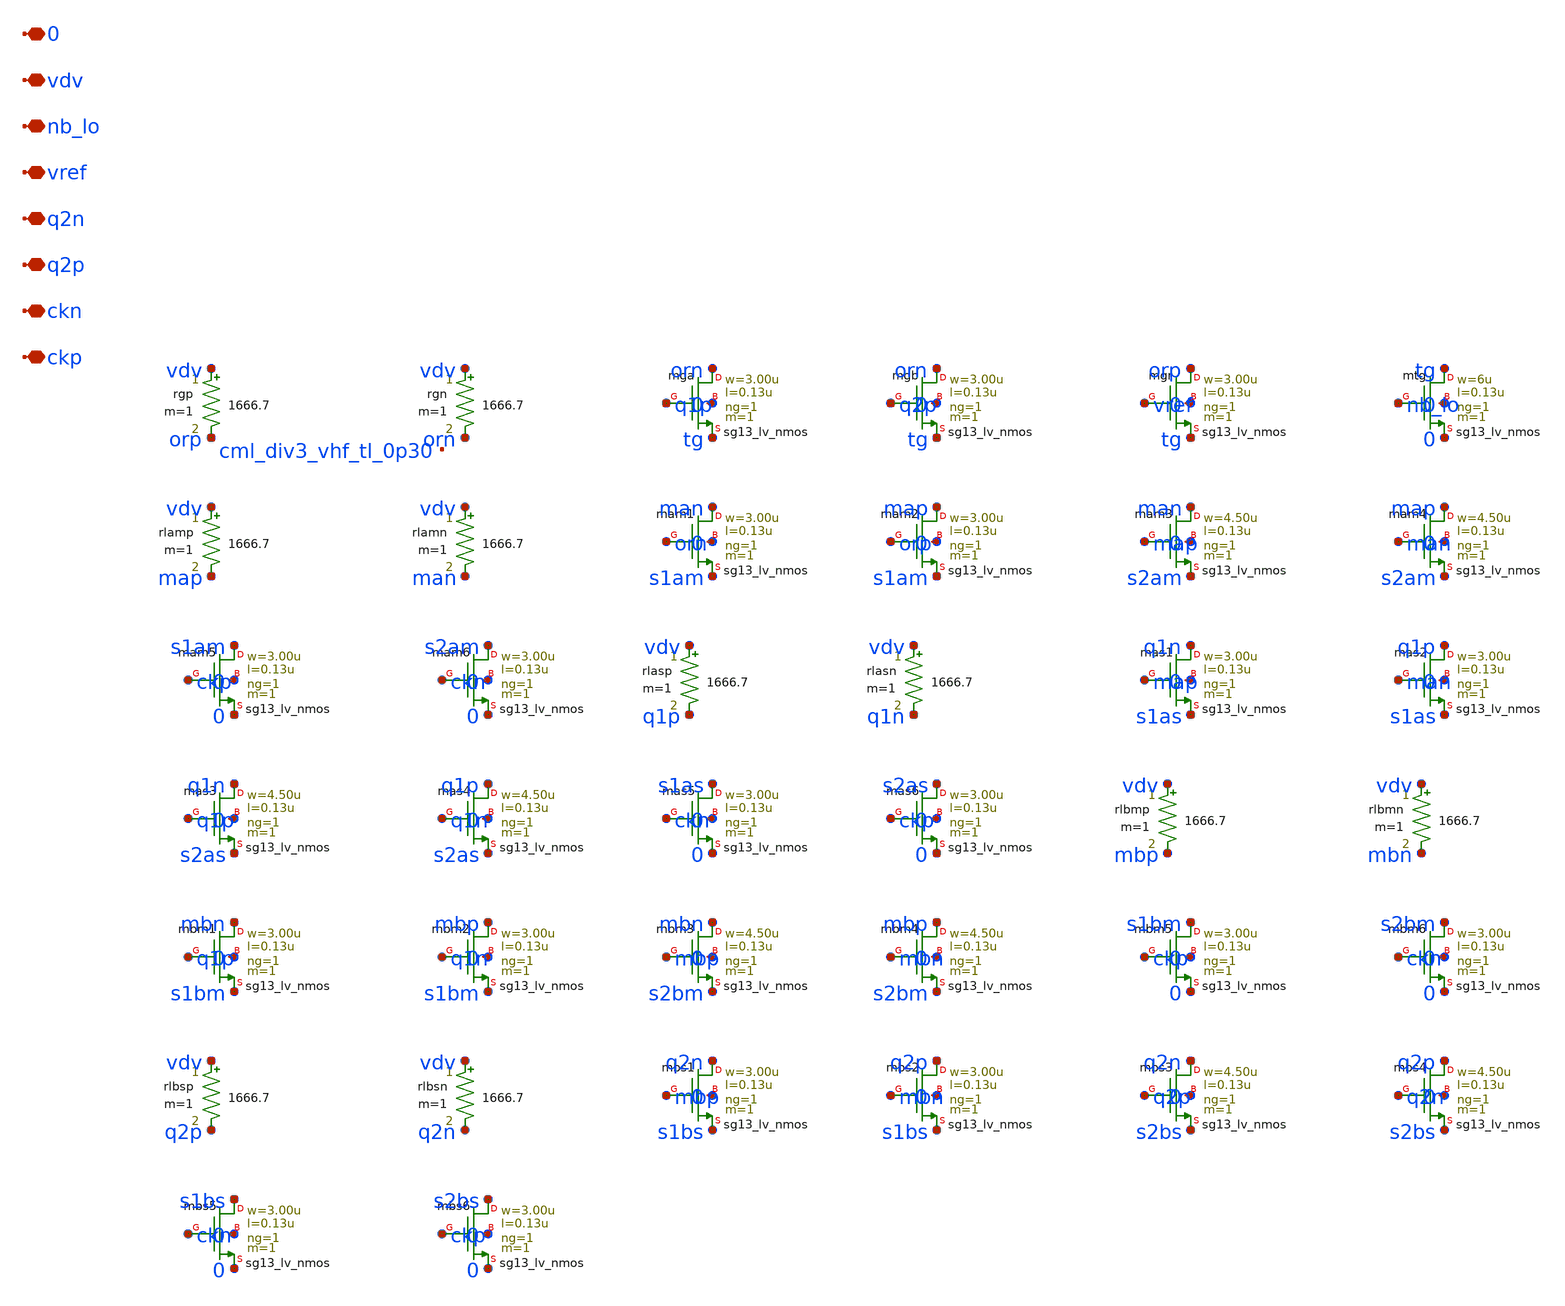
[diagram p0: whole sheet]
** sch_path: analog/lo/sch/cml_div3_vhf.sch
**.subckt cml_div3_vhf ckp ckn q2p q2n vref nb_lo vdv 0
*.iopin ckp
*.iopin ckn
*.iopin q2p
*.iopin q2n
*.iopin vref
*.iopin nb_lo
*.iopin vdv
*.iopin 0
rgp vdv orp 1666.7 m=1
rgn vdv orn 1666.7 m=1
Xmga orn q1p tg 0 sg13_lv_nmos w=3.00u l=0.13u ng=1 m=1 mm_ok=1
Xmgb orn q2p tg 0 sg13_lv_nmos w=3.00u l=0.13u ng=1 m=1 mm_ok=1
Xmgr orp vref tg 0 sg13_lv_nmos w=3.00u l=0.13u ng=1 m=1 mm_ok=1
Xmtg tg nb_lo 0 0 sg13_lv_nmos w=6u l=0.13u ng=1 m=1 mm_ok=1
rlamp vdv map 1666.7 m=1
rlamn vdv man 1666.7 m=1
Xmam1 man orn s1am 0 sg13_lv_nmos w=3.00u l=0.13u ng=1 m=1 mm_ok=1
Xmam2 map orp s1am 0 sg13_lv_nmos w=3.00u l=0.13u ng=1 m=1 mm_ok=1
Xmam3 man map s2am 0 sg13_lv_nmos w=4.50u l=0.13u ng=1 m=1 mm_ok=1
Xmam4 map man s2am 0 sg13_lv_nmos w=4.50u l=0.13u ng=1 m=1 mm_ok=1
Xmam5 s1am ckp 0 0 sg13_lv_nmos w=3.00u l=0.13u ng=1 m=1 mm_ok=1
Xmam6 s2am ckn 0 0 sg13_lv_nmos w=3.00u l=0.13u ng=1 m=1 mm_ok=1
rlasp vdv q1p 1666.7 m=1
rlasn vdv q1n 1666.7 m=1
Xmas1 q1n map s1as 0 sg13_lv_nmos w=3.00u l=0.13u ng=1 m=1 mm_ok=1
Xmas2 q1p man s1as 0 sg13_lv_nmos w=3.00u l=0.13u ng=1 m=1 mm_ok=1
Xmas3 q1n q1p s2as 0 sg13_lv_nmos w=4.50u l=0.13u ng=1 m=1 mm_ok=1
Xmas4 q1p q1n s2as 0 sg13_lv_nmos w=4.50u l=0.13u ng=1 m=1 mm_ok=1
Xmas5 s1as ckn 0 0 sg13_lv_nmos w=3.00u l=0.13u ng=1 m=1 mm_ok=1
Xmas6 s2as ckp 0 0 sg13_lv_nmos w=3.00u l=0.13u ng=1 m=1 mm_ok=1
rlbmp vdv mbp 1666.7 m=1
rlbmn vdv mbn 1666.7 m=1
Xmbm1 mbn q1p s1bm 0 sg13_lv_nmos w=3.00u l=0.13u ng=1 m=1 mm_ok=1
Xmbm2 mbp q1n s1bm 0 sg13_lv_nmos w=3.00u l=0.13u ng=1 m=1 mm_ok=1
Xmbm3 mbn mbp s2bm 0 sg13_lv_nmos w=4.50u l=0.13u ng=1 m=1 mm_ok=1
Xmbm4 mbp mbn s2bm 0 sg13_lv_nmos w=4.50u l=0.13u ng=1 m=1 mm_ok=1
Xmbm5 s1bm ckp 0 0 sg13_lv_nmos w=3.00u l=0.13u ng=1 m=1 mm_ok=1
Xmbm6 s2bm ckn 0 0 sg13_lv_nmos w=3.00u l=0.13u ng=1 m=1 mm_ok=1
rlbsp vdv q2p 1666.7 m=1
rlbsn vdv q2n 1666.7 m=1
Xmbs1 q2n mbp s1bs 0 sg13_lv_nmos w=3.00u l=0.13u ng=1 m=1 mm_ok=1
Xmbs2 q2p mbn s1bs 0 sg13_lv_nmos w=3.00u l=0.13u ng=1 m=1 mm_ok=1
Xmbs3 q2n q2p s2bs 0 sg13_lv_nmos w=4.50u l=0.13u ng=1 m=1 mm_ok=1
Xmbs4 q2p q2n s2bs 0 sg13_lv_nmos w=4.50u l=0.13u ng=1 m=1 mm_ok=1
Xmbs5 s1bs ckn 0 0 sg13_lv_nmos w=3.00u l=0.13u ng=1 m=1 mm_ok=1
Xmbs6 s2bs ckp 0 0 sg13_lv_nmos w=3.00u l=0.13u ng=1 m=1 mm_ok=1
**.ends
.end
